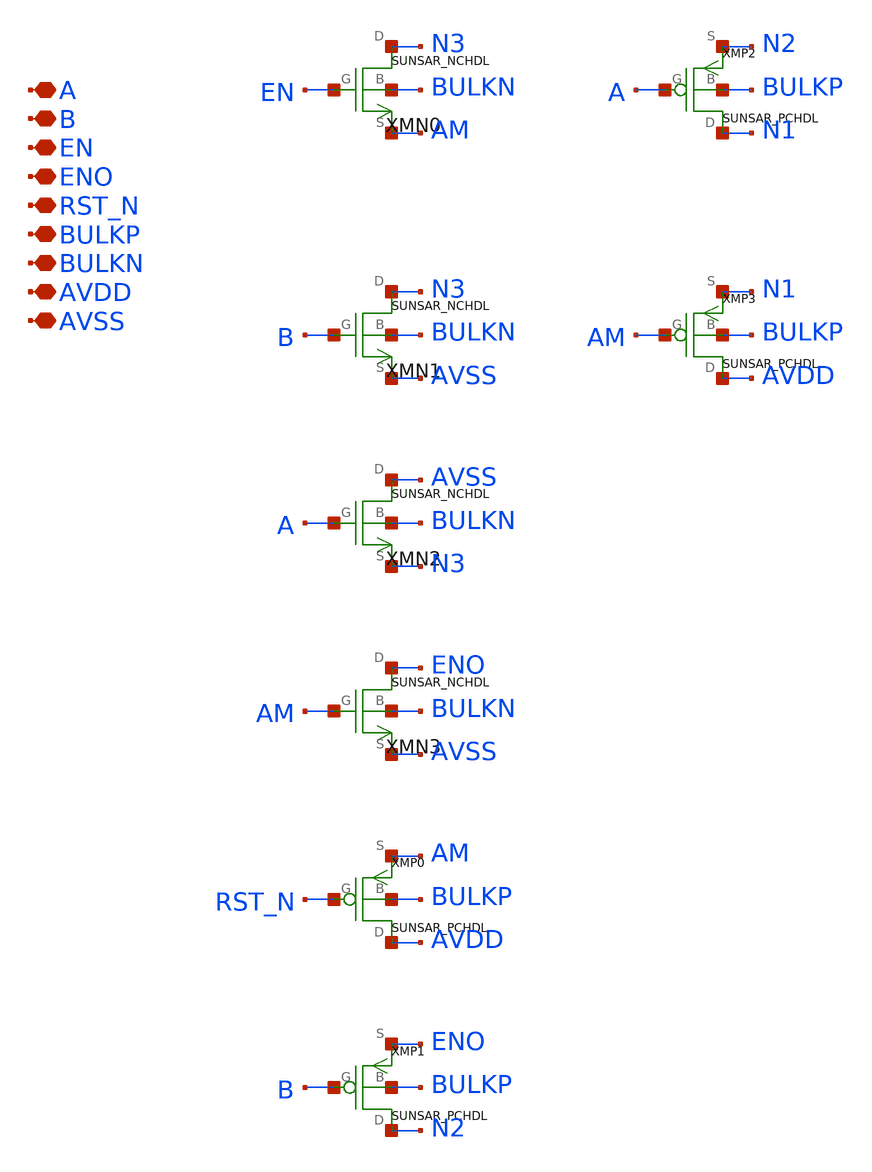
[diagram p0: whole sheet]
** sch_path: ip/sun_sar9b_sky130nm/design/SUN_SAR9B_SKY130NM/SUNSAR_SAREMX1_CV.sch
**.subckt SUNSAR_SAREMX1_CV A B EN ENO RST_N BULKP BULKN AVDD AVSS
*.iopin A
*.iopin B
*.iopin EN
*.iopin ENO
*.iopin RST_N
*.iopin BULKP
*.iopin BULKN
*.iopin AVDD
*.iopin AVSS
XMN0 N3 EN AM BULKN SUNSAR_NCHDL
XMN1 N3 B AVSS BULKN SUNSAR_NCHDL
XMN2 AVSS A N3 BULKN SUNSAR_NCHDL
XMN3 ENO AM AVSS BULKN SUNSAR_NCHDL
XMP0 AVDD RST_N AM BULKP SUNSAR_PCHDL
XMP1 N2 B ENO BULKP SUNSAR_PCHDL
XMP2 N1 A N2 BULKP SUNSAR_PCHDL
XMP3 AVDD AM N1 BULKP SUNSAR_PCHDL
**.ends
.end
